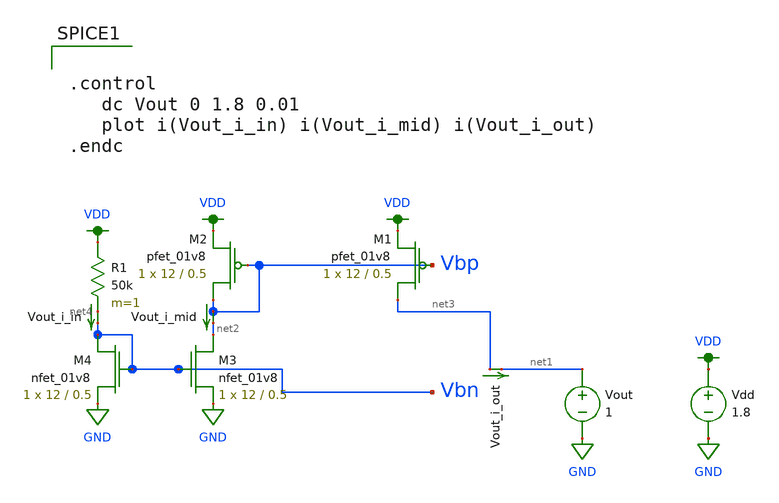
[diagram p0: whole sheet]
** sch_path: test_harness_current_mirror.sch
**.subckt test_harness_current_mirror
Vout net1 GND 1
XM2 Vbp Vbp VDD VDD sky130_fd_pr__pfet_01v8 L=0.5 W=12 nf=1 ad='int((nf+1)/2) * W/nf * 0.29' as='int((nf+2)/2) * W/nf * 0.29'
+ pd='2*int((nf+1)/2) * (W/nf + 0.29)' ps='2*int((nf+2)/2) * (W/nf + 0.29)' nrd='0.29 / W' nrs='0.29 / W'
+ sa=0 sb=0 sd=0 mult=1 m=1
XM4 Vbn Vbn GND GND sky130_fd_pr__nfet_01v8 L=0.5 W=12 nf=1 ad='int((nf+1)/2) * W/nf * 0.29' as='int((nf+2)/2) * W/nf * 0.29'
+ pd='2*int((nf+1)/2) * (W/nf + 0.29)' ps='2*int((nf+2)/2) * (W/nf + 0.29)' nrd='0.29 / W' nrs='0.29 / W'
+ sa=0 sb=0 sd=0 mult=1 m=1
Vout_i_in net4 Vbn 0
.save i(vout_i_in)
Vout_i_mid Vbp net2 0
.save i(vout_i_mid)
Vout_i_out net3 net1 0
.save i(vout_i_out)
Vdd VDD GND 1.8
R1 VDD net4 50k m=1
XM3 net2 Vbn GND GND sky130_fd_pr__nfet_01v8 L=0.5 W=12 nf=1 ad='int((nf+1)/2) * W/nf * 0.29' as='int((nf+2)/2) * W/nf * 0.29'
+ pd='2*int((nf+1)/2) * (W/nf + 0.29)' ps='2*int((nf+2)/2) * (W/nf + 0.29)' nrd='0.29 / W' nrs='0.29 / W'
+ sa=0 sb=0 sd=0 mult=1 m=1
XM1 net3 Vbp VDD VDD sky130_fd_pr__pfet_01v8 L=0.5 W=12 nf=1 ad='int((nf+1)/2) * W/nf * 0.29' as='int((nf+2)/2) * W/nf * 0.29'
+ pd='2*int((nf+1)/2) * (W/nf + 0.29)' ps='2*int((nf+2)/2) * (W/nf + 0.29)' nrd='0.29 / W' nrs='0.29 / W'
+ sa=0 sb=0 sd=0 mult=1 m=1
**** begin user architecture code


.control
   dc Vout 0 1.8 0.01
   plot i(Vout_i_in) i(Vout_i_mid) i(Vout_i_out)
.endc


.option wnflag=1
.param MC_SWITCH=0.0
.lib ~/skywater/skywater-pdk/libraries/sky130_fd_pr_ngspice/latest/models/sky130.lib.spice tt

**** end user architecture code
**.ends
.GLOBAL GND
.GLOBAL VDD
.end
